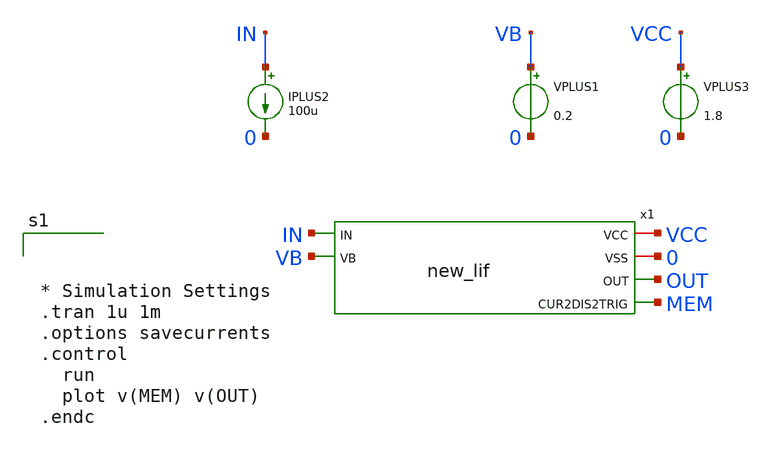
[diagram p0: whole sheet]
** sch_path: xschem/tb_new_lif.sch
**.subckt tb_new_lif
x1 VCC 0 IN OUT VB MEM new_lif
VPLUS1 VB 0 0.2
VPLUS3 VCC 0 1.8
IPLUS2 IN 0 100u
**** begin user architecture code

** opencircuitdesign pdks install
.lib $::SKYWATER_MODELS/sky130.lib.spice tt





* Simulation Settings
.tran 1u 1m
.options savecurrents
.control
  run
  plot v(MEM) v(OUT)
.endc


**** end user architecture code
**.ends

* expanding   symbol:  new_lif.sym # of pins=6
** sym_path: xschem/new_lif.sym
** sch_path: xschem/new_lif.sch
.subckt new_lif VCC VSS IN OUT VB CUR2DIS2TRIG
*.iopin VCC
*.iopin VSS
*.ipin IN
*.opin OUT
*.ipin VB
*.opin CUR2DIS2TRIG
XM1 IN IN VCC VCC sky130_fd_pr__pfet_01v8 L=0.15 W=1 nf=1 ad='int((nf+1)/2) * W/nf * 0.29' as='int((nf+2)/2) * W/nf * 0.29'
+ pd='2*int((nf+1)/2) * (W/nf + 0.29)' ps='2*int((nf+2)/2) * (W/nf + 0.29)' nrd='0.29 / W' nrs='0.29 / W'
+ sa=0 sb=0 sd=0 mult=1 m=1
XM4 RST2DIS RST2DIS net3 VSS sky130_fd_pr__nfet_01v8 L=0.15 W=1 nf=1 ad='int((nf+1)/2) * W/nf * 0.29'
+ as='int((nf+2)/2) * W/nf * 0.29' pd='2*int((nf+1)/2) * (W/nf + 0.29)' ps='2*int((nf+2)/2) * (W/nf + 0.29)'
+ nrd='0.29 / W' nrs='0.29 / W' sa=0 sb=0 sd=0 mult=1 m=1
XM2 CUR2DIS2TRIG IN VCC VCC sky130_fd_pr__pfet_01v8 L=0.15 W=1 nf=1 ad='int((nf+1)/2) * W/nf * 0.29'
+ as='int((nf+2)/2) * W/nf * 0.29' pd='2*int((nf+1)/2) * (W/nf + 0.29)' ps='2*int((nf+2)/2) * (W/nf + 0.29)'
+ nrd='0.29 / W' nrs='0.29 / W' sa=0 sb=0 sd=0 mult=1 m=1
XM3 RST2TRIG2BUF CUR2DIS2TRIG VCC VCC sky130_fd_pr__pfet_01v8 L=0.15 W=1 nf=1 ad='int((nf+1)/2) * W/nf * 0.29'
+ as='int((nf+2)/2) * W/nf * 0.29' pd='2*int((nf+1)/2) * (W/nf + 0.29)' ps='2*int((nf+2)/2) * (W/nf + 0.29)'
+ nrd='0.29 / W' nrs='0.29 / W' sa=0 sb=0 sd=0 mult=1 m=1
XM5 net1 RST2TRIG2BUF VCC VCC sky130_fd_pr__pfet_01v8 L=0.15 W=1 nf=1 ad='int((nf+1)/2) * W/nf * 0.29'
+ as='int((nf+2)/2) * W/nf * 0.29' pd='2*int((nf+1)/2) * (W/nf + 0.29)' ps='2*int((nf+2)/2) * (W/nf + 0.29)'
+ nrd='0.29 / W' nrs='0.29 / W' sa=0 sb=0 sd=0 mult=1 m=1
XM6 RST2TRIG2BUF CUR2DIS2TRIG net2 VSS sky130_fd_pr__nfet_01v8 L=0.15 W=1 nf=1 ad='int((nf+1)/2) * W/nf * 0.29'
+ as='int((nf+2)/2) * W/nf * 0.29' pd='2*int((nf+1)/2) * (W/nf + 0.29)' ps='2*int((nf+2)/2) * (W/nf + 0.29)'
+ nrd='0.29 / W' nrs='0.29 / W' sa=0 sb=0 sd=0 mult=1 m=1
XM7 net1 RST2TRIG2BUF net2 VSS sky130_fd_pr__nfet_01v8 L=0.15 W=1 nf=1 ad='int((nf+1)/2) * W/nf * 0.29'
+ as='int((nf+2)/2) * W/nf * 0.29' pd='2*int((nf+1)/2) * (W/nf + 0.29)' ps='2*int((nf+2)/2) * (W/nf + 0.29)'
+ nrd='0.29 / W' nrs='0.29 / W' sa=0 sb=0 sd=0 mult=1 m=1
XM8 net2 net1 VSS VSS sky130_fd_pr__nfet_01v8 L=0.15 W=1 nf=1 ad='int((nf+1)/2) * W/nf * 0.29' as='int((nf+2)/2) * W/nf * 0.29'
+ pd='2*int((nf+1)/2) * (W/nf + 0.29)' ps='2*int((nf+2)/2) * (W/nf + 0.29)' nrd='0.29 / W' nrs='0.29 / W'
+ sa=0 sb=0 sd=0 mult=1 m=1
XM9 OUT RST2TRIG2BUF VCC VCC sky130_fd_pr__pfet_01v8 L=0.15 W=1 nf=1 ad='int((nf+1)/2) * W/nf * 0.29'
+ as='int((nf+2)/2) * W/nf * 0.29' pd='2*int((nf+1)/2) * (W/nf + 0.29)' ps='2*int((nf+2)/2) * (W/nf + 0.29)'
+ nrd='0.29 / W' nrs='0.29 / W' sa=0 sb=0 sd=0 mult=1 m=1
XM10 OUT RST2TRIG2BUF VSS VSS sky130_fd_pr__nfet_01v8 L=0.15 W=1 nf=1 ad='int((nf+1)/2) * W/nf * 0.29'
+ as='int((nf+2)/2) * W/nf * 0.29' pd='2*int((nf+1)/2) * (W/nf + 0.29)' ps='2*int((nf+2)/2) * (W/nf + 0.29)'
+ nrd='0.29 / W' nrs='0.29 / W' sa=0 sb=0 sd=0 mult=1 m=1
XM11 net4 RST2TRIG2BUF VCC VCC sky130_fd_pr__pfet_01v8 L=0.15 W=1 nf=1 ad='int((nf+1)/2) * W/nf * 0.29'
+ as='int((nf+2)/2) * W/nf * 0.29' pd='2*int((nf+1)/2) * (W/nf + 0.29)' ps='2*int((nf+2)/2) * (W/nf + 0.29)'
+ nrd='0.29 / W' nrs='0.29 / W' sa=0 sb=0 sd=0 mult=1 m=1
XM12 RST2DIS RST2DIS net4 VCC sky130_fd_pr__pfet_01v8 L=0.15 W=1 nf=1 ad='int((nf+1)/2) * W/nf * 0.29'
+ as='int((nf+2)/2) * W/nf * 0.29' pd='2*int((nf+1)/2) * (W/nf + 0.29)' ps='2*int((nf+2)/2) * (W/nf + 0.29)'
+ nrd='0.29 / W' nrs='0.29 / W' sa=0 sb=0 sd=0 mult=1 m=1
XM13 net3 VB VSS VSS sky130_fd_pr__nfet_01v8 L=0.15 W=1 nf=1 ad='int((nf+1)/2) * W/nf * 0.29' as='int((nf+2)/2) * W/nf * 0.29'
+ pd='2*int((nf+1)/2) * (W/nf + 0.29)' ps='2*int((nf+2)/2) * (W/nf + 0.29)' nrd='0.29 / W' nrs='0.29 / W'
+ sa=0 sb=0 sd=0 mult=1 m=1
XM14 CUR2DIS2TRIG RST2DIS VSS VSS sky130_fd_pr__nfet_01v8 L=0.15 W=1 nf=1 ad='int((nf+1)/2) * W/nf * 0.29'
+ as='int((nf+2)/2) * W/nf * 0.29' pd='2*int((nf+1)/2) * (W/nf + 0.29)' ps='2*int((nf+2)/2) * (W/nf + 0.29)'
+ nrd='0.29 / W' nrs='0.29 / W' sa=0 sb=0 sd=0 mult=1 m=1
XC1 CUR2DIS2TRIG VSS sky130_fd_pr__cap_mim_m3_1 W=1 L=1 MF=12 m=12
XM15 CUR2DIS2TRIG VB VSS VSS sky130_fd_pr__nfet_01v8 L=0.15 W=1 nf=1 ad='int((nf+1)/2) * W/nf * 0.29'
+ as='int((nf+2)/2) * W/nf * 0.29' pd='2*int((nf+1)/2) * (W/nf + 0.29)' ps='2*int((nf+2)/2) * (W/nf + 0.29)'
+ nrd='0.29 / W' nrs='0.29 / W' sa=0 sb=0 sd=0 mult=1 m=1
.ends

.end
